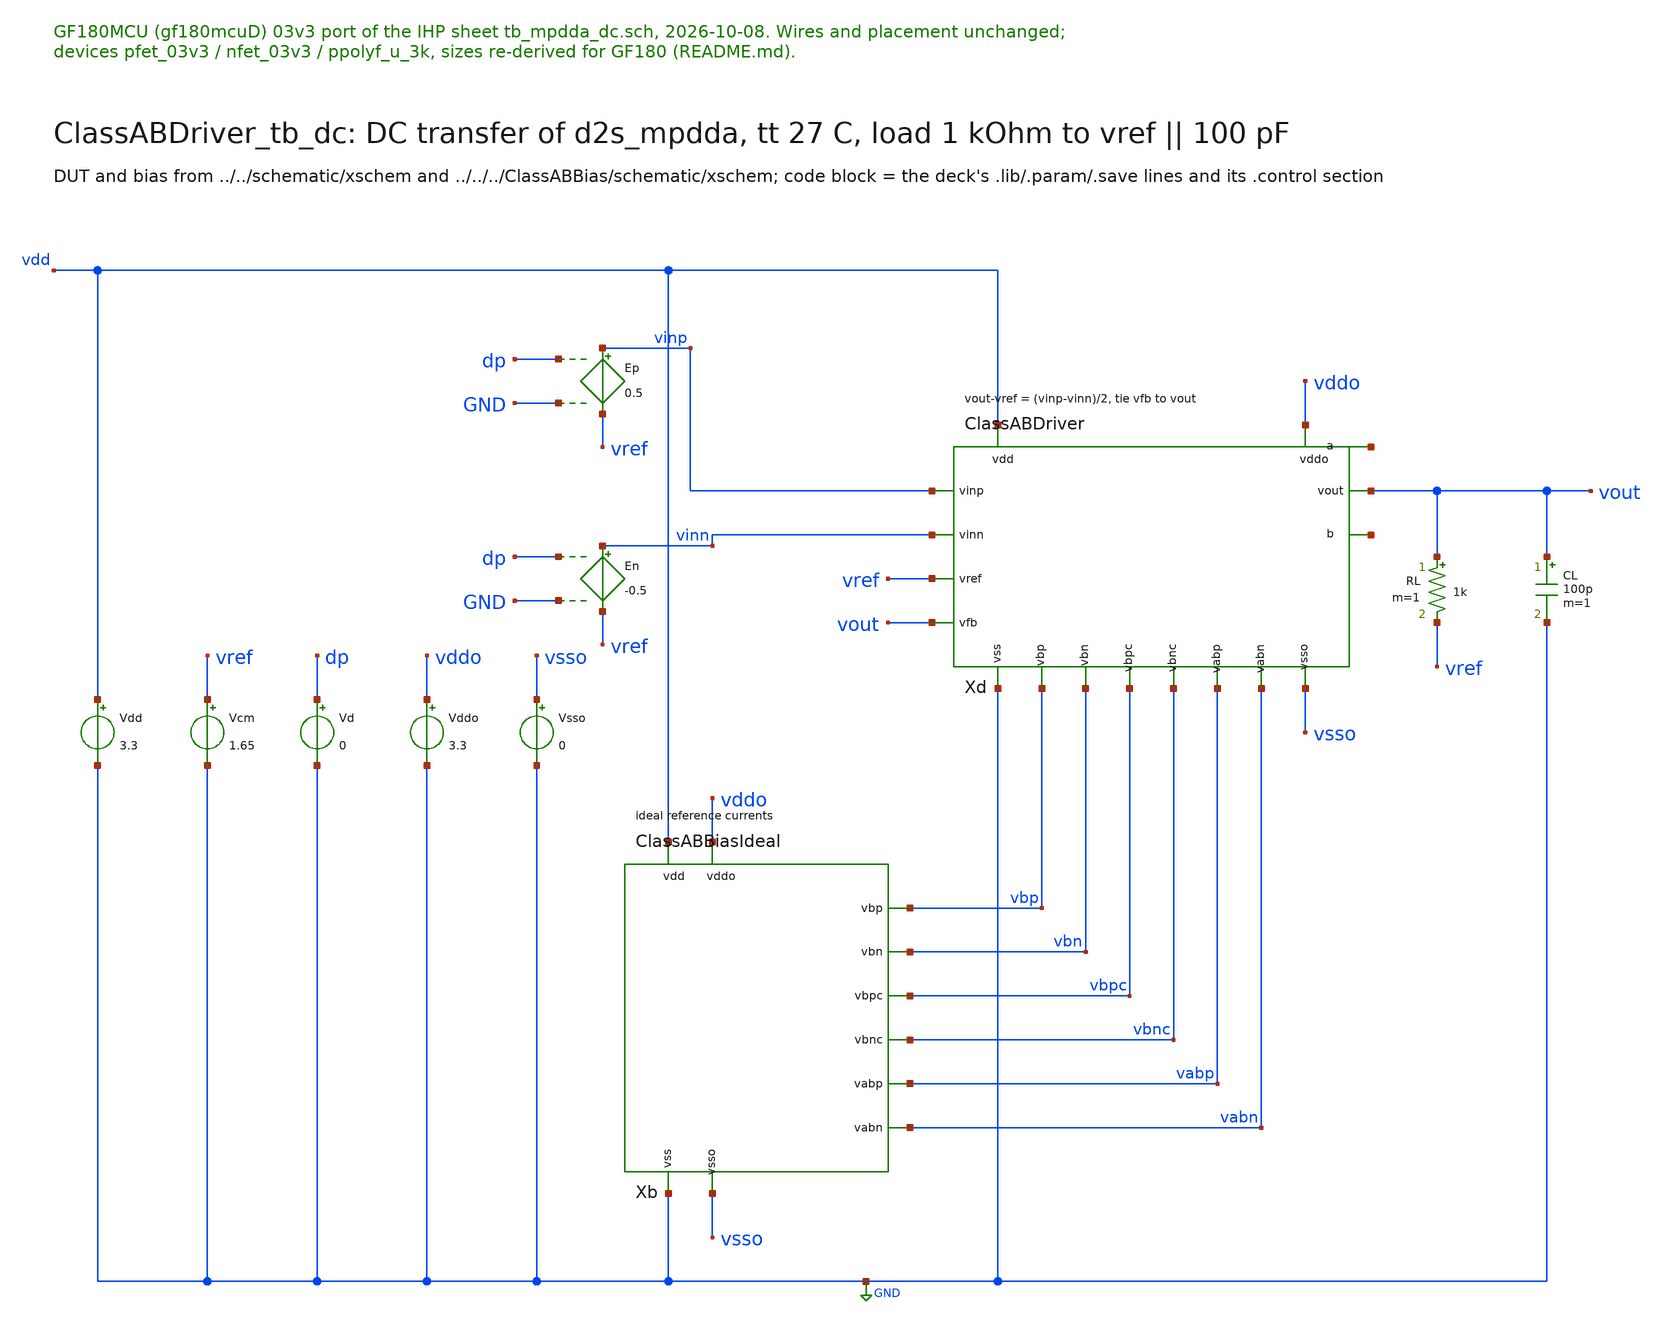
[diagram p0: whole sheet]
** sch_path: macros/ClassABDriver/testbenches/xschem/ClassABDriver_tb_dc.sch
**.subckt ClassABDriver_tb_dc
Vdd vdd GND 3.3
Vcm vref GND 1.65
Xb vdd GND vddo vsso vbp vbn vbpc vbnc vabp vabn ClassABBiasIdeal
Xd vdd GND vddo vsso vinp vinn vref vout vout vbp vbn vbpc vbnc vabp vabn net1 net2 ClassABDriver
Vd dp GND 0
Ep vinp vref dp GND 0.5
En vinn vref dp GND -0.5
RL vout vref 1k m=1
CL vout GND 100p m=1
Vddo vddo GND 3.3
Vsso vsso GND 0
**** begin user architecture code

.param vstep=0.5
.save v(vout) v(dp) vdd#branch vddo#branch @m.xd.xop.m0[id] @m.xd.xon.m0[id]
.control
dc Vd -1 1 0.01
let vo = v(vout) - 1.65
let ip = abs(@m.xd.xop.m0[id])
let in = abs(@m.xd.xon.m0[id])
let idd = -i(vdd) - i(vddo)
meas dc vop find vo at=0.2
meas dc von find vo at=-0.2
meas dc off find vo at=0
meas dc iqp find ip at=0
meas dc iqn find in at=0
meas dc iddq find idd at=0
let gain = (vop - von)/0.4
let err = vo - gain*v(dp) - off
let nonlin = vecmax(abs(err))
print gain off nonlin iqp iqn iddq
if $?batchmode = 0
  plot vo
  plot err
end
.endc


.include $::180MCU_MODELS/design.ngspice
.lib $::180MCU_MODELS/sm141064.ngspice typical
.lib $::180MCU_MODELS/sm141064.ngspice res_typical
.lib $::180MCU_MODELS/sm141064.ngspice moscap_typical

**** end user architecture code
**.ends
.GLOBAL GND
.end
